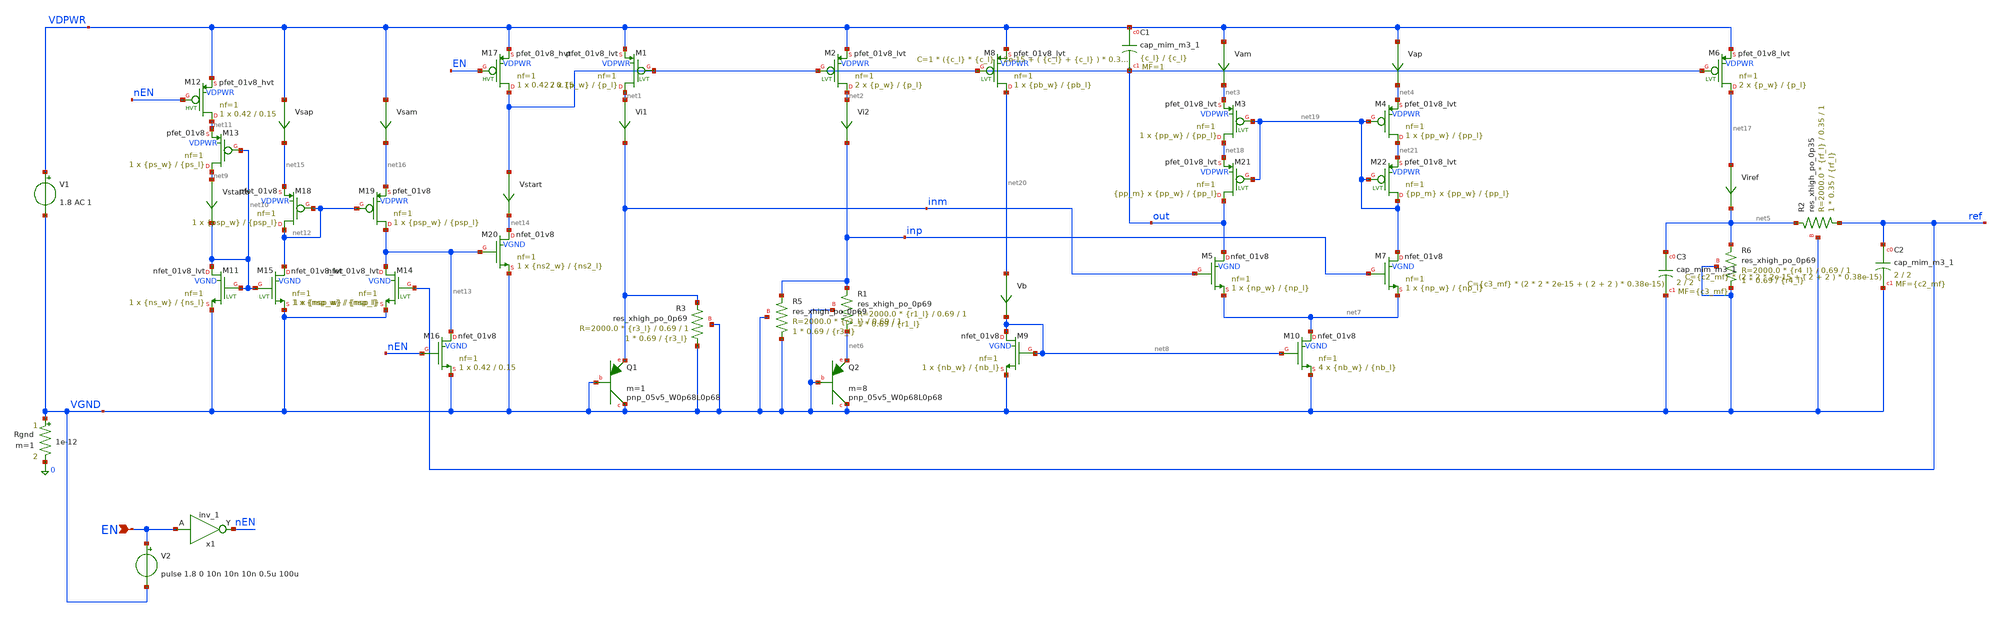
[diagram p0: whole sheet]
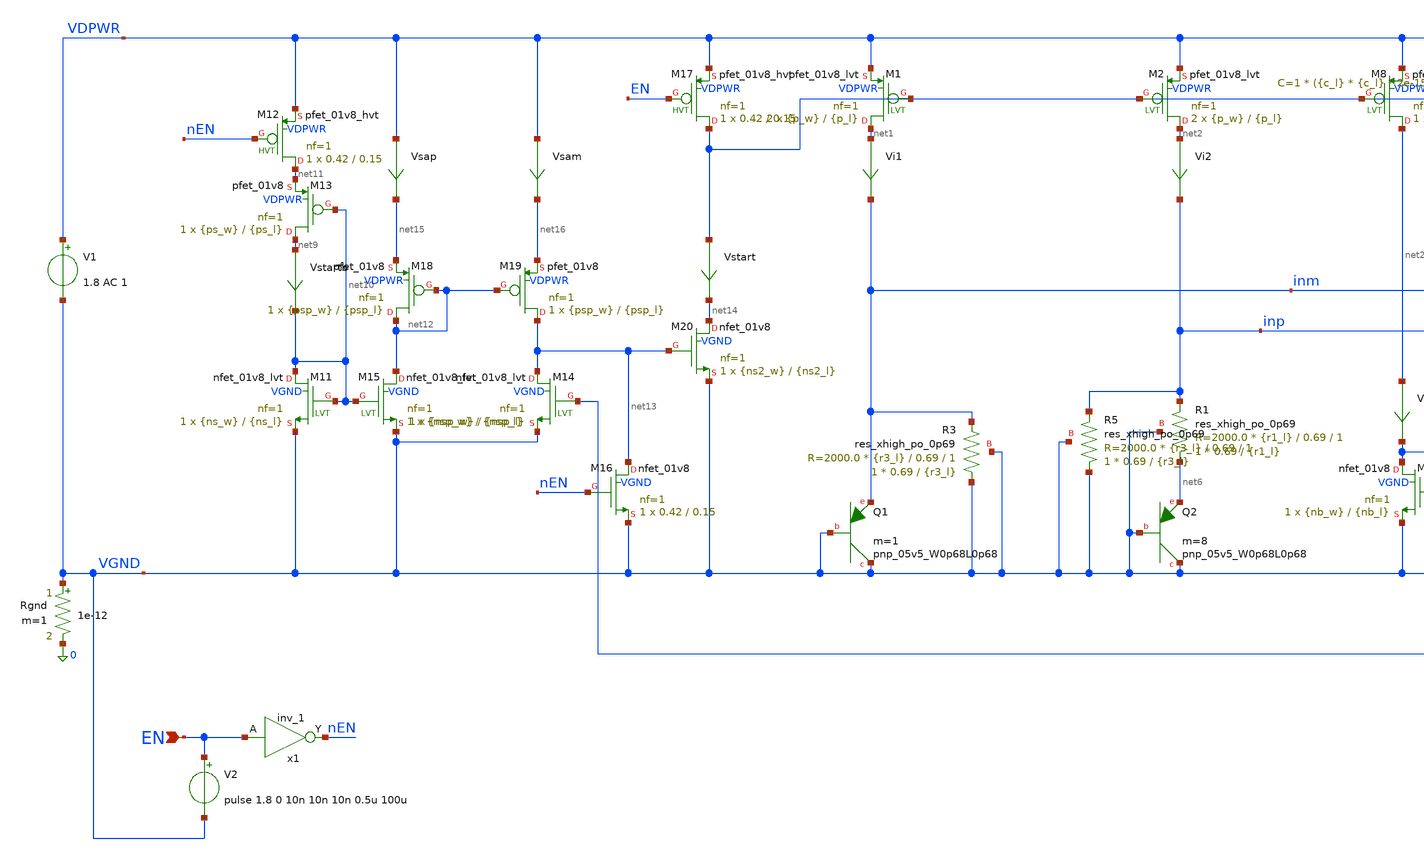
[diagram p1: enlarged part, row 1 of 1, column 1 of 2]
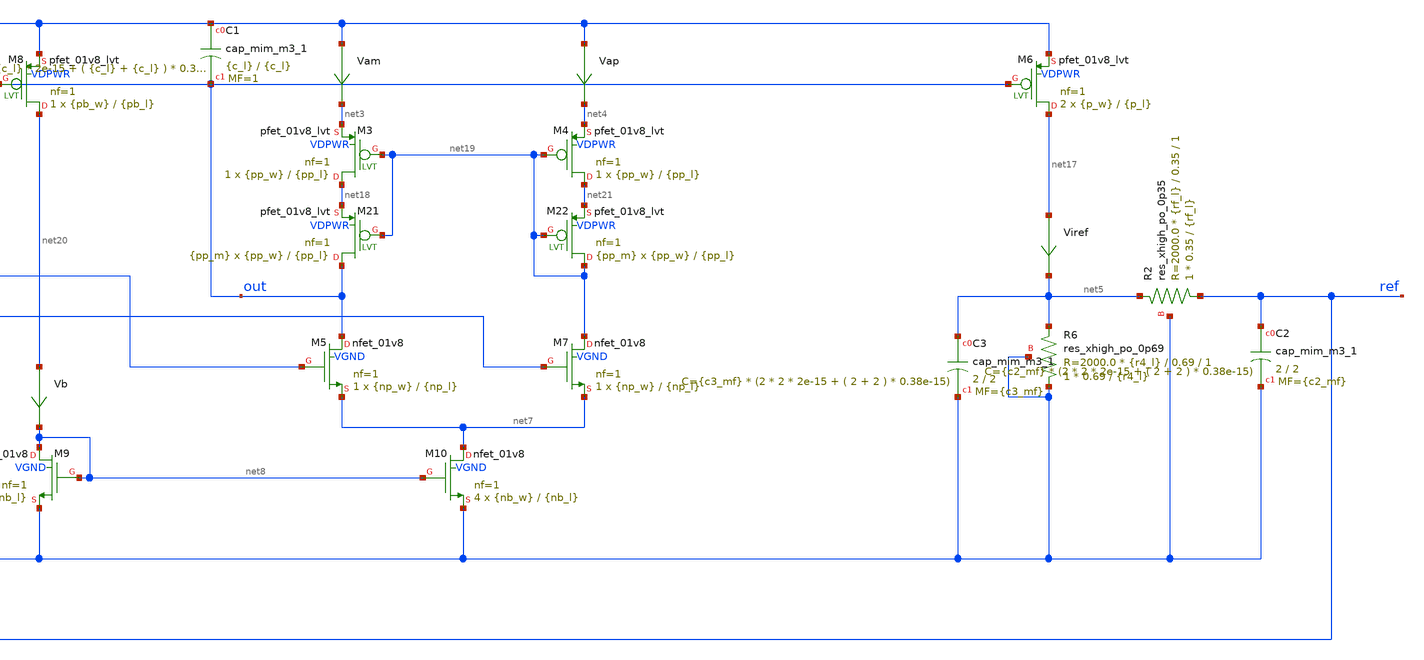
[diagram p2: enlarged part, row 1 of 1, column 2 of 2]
** sch_path: xschem/bgr.sch
**.subckt bgr EN
*.ipin EN
XQ1 VGND VGND inm sky130_fd_pr__pnp_05v5_W0p68L0p68 m=1
Rgnd VGND 0 1e-12 m=1
V1 VDPWR VGND 1.8 AC 1
XR1 net6 inp VGND sky130_fd_pr__res_xhigh_po_0p69 L={r1_l} mult=1 m=1
XQ2 VGND VGND net6 sky130_fd_pr__pnp_05v5_W0p68L0p68 m=8
XM1 net1 out VDPWR VDPWR sky130_fd_pr__pfet_01v8_lvt L={p_l} W={p_w} nf=1 ad='int((1 + 1)/2) * {p_w} / 1 * 0.29'
+ as='int((1 + 2)/2) * {p_w} / 1 * 0.29' pd='2*int((1 + 1)/2) * ({p_w} / 1 + 0.29)' ps='2*int((1 + 2)/2) * ({p_w} / 1 + 0.29)'
+ nrd='0.29 / {p_w} ' nrs='0.29 / {p_w} ' sa=0 sb=0 sd=0 mult=2 m=2
XM2 net2 out VDPWR VDPWR sky130_fd_pr__pfet_01v8_lvt L={p_l} W={p_w} nf=1 ad='int((1 + 1)/2) * {p_w} / 1 * 0.29'
+ as='int((1 + 2)/2) * {p_w} / 1 * 0.29' pd='2*int((1 + 1)/2) * ({p_w} / 1 + 0.29)' ps='2*int((1 + 2)/2) * ({p_w} / 1 + 0.29)'
+ nrd='0.29 / {p_w} ' nrs='0.29 / {p_w} ' sa=0 sb=0 sd=0 mult=2 m=2
XM3 net18 net19 net3 VDPWR sky130_fd_pr__pfet_01v8_lvt L={pp_l} W={pp_w} nf=1 ad='int((1 + 1)/2) * {pp_w} / 1 * 0.29'
+ as='int((1 + 2)/2) * {pp_w} / 1 * 0.29' pd='2*int((1 + 1)/2) * ({pp_w} / 1 + 0.29)' ps='2*int((1 + 2)/2) * ({pp_w} / 1 + 0.29)'
+ nrd='0.29 / {pp_w} ' nrs='0.29 / {pp_w} ' sa=0 sb=0 sd=0 mult=1 m=1
XM4 net21 net19 net4 VDPWR sky130_fd_pr__pfet_01v8_lvt L={pp_l} W={pp_w} nf=1 ad='int((1 + 1)/2) * {pp_w} / 1 * 0.29'
+ as='int((1 + 2)/2) * {pp_w} / 1 * 0.29' pd='2*int((1 + 1)/2) * ({pp_w} / 1 + 0.29)' ps='2*int((1 + 2)/2) * ({pp_w} / 1 + 0.29)'
+ nrd='0.29 / {pp_w} ' nrs='0.29 / {pp_w} ' sa=0 sb=0 sd=0 mult=1 m=1
XM7 net19 inp net7 VGND sky130_fd_pr__nfet_01v8 L={np_l} W={np_w} nf=1 ad='int((1 + 1)/2) * {np_w} / 1 * 0.29'
+ as='int((1 + 2)/2) * {np_w} / 1 * 0.29' pd='2*int((1 + 1)/2) * ({np_w} / 1 + 0.29)' ps='2*int((1 + 2)/2) * ({np_w} / 1 + 0.29)'
+ nrd='0.29 / {np_w} ' nrs='0.29 / {np_w} ' sa=0 sb=0 sd=0 mult=1 m=1
Vi1 net1 inm 0
.save i(vi1)
Vi2 net2 inp 0
.save i(vi2)
Vam VDPWR net3 0
.save i(vam)
Vap VDPWR net4 0
.save i(vap)
XR3 VGND inm VGND sky130_fd_pr__res_xhigh_po_0p69 L={r3_l} mult=1 m=1
XR5 VGND inp VGND sky130_fd_pr__res_xhigh_po_0p69 L={r3_l} mult=1 m=1
XM5 out inm net7 VGND sky130_fd_pr__nfet_01v8 L={np_l} W={np_w} nf=1 ad='int((1 + 1)/2) * {np_w} / 1 * 0.29'
+ as='int((1 + 2)/2) * {np_w} / 1 * 0.29' pd='2*int((1 + 1)/2) * ({np_w} / 1 + 0.29)' ps='2*int((1 + 2)/2) * ({np_w} / 1 + 0.29)'
+ nrd='0.29 / {np_w} ' nrs='0.29 / {np_w} ' sa=0 sb=0 sd=0 mult=1 m=1
XM6 net17 out VDPWR VDPWR sky130_fd_pr__pfet_01v8_lvt L={p_l} W={p_w} nf=1 ad='int((1 + 1)/2) * {p_w} / 1 * 0.29'
+ as='int((1 + 2)/2) * {p_w} / 1 * 0.29' pd='2*int((1 + 1)/2) * ({p_w} / 1 + 0.29)' ps='2*int((1 + 2)/2) * ({p_w} / 1 + 0.29)'
+ nrd='0.29 / {p_w} ' nrs='0.29 / {p_w} ' sa=0 sb=0 sd=0 mult=2 m=2
XR6 VGND net5 VGND sky130_fd_pr__res_xhigh_po_0p69 L={r4_l} mult=1 m=1
Viref net17 net5 0
.save i(viref)
XM8 net20 out VDPWR VDPWR sky130_fd_pr__pfet_01v8_lvt L={pb_l} W={pb_w} nf=1 ad='int((1 + 1)/2) * {pb_w} / 1 * 0.29'
+ as='int((1 + 2)/2) * {pb_w} / 1 * 0.29' pd='2*int((1 + 1)/2) * ({pb_w} / 1 + 0.29)' ps='2*int((1 + 2)/2) * ({pb_w} / 1 + 0.29)'
+ nrd='0.29 / {pb_w} ' nrs='0.29 / {pb_w} ' sa=0 sb=0 sd=0 mult=1 m=1
XM9 net8 net8 VGND VGND sky130_fd_pr__nfet_01v8 L={nb_l} W={nb_w} nf=1 ad='int((1 + 1)/2) * {nb_w} / 1 * 0.29'
+ as='int((1 + 2)/2) * {nb_w} / 1 * 0.29' pd='2*int((1 + 1)/2) * ({nb_w} / 1 + 0.29)' ps='2*int((1 + 2)/2) * ({nb_w} / 1 + 0.29)'
+ nrd='0.29 / {nb_w} ' nrs='0.29 / {nb_w} ' sa=0 sb=0 sd=0 mult=1 m=1
XM10 net7 net8 VGND VGND sky130_fd_pr__nfet_01v8 L={nb_l} W={nb_w} nf=1 ad='int((1 + 1)/2) * {nb_w} / 1 * 0.29'
+ as='int((1 + 2)/2) * {nb_w} / 1 * 0.29' pd='2*int((1 + 1)/2) * ({nb_w} / 1 + 0.29)' ps='2*int((1 + 2)/2) * ({nb_w} / 1 + 0.29)'
+ nrd='0.29 / {nb_w} ' nrs='0.29 / {nb_w} ' sa=0 sb=0 sd=0 mult=4 m=4
Vb net20 net8 0
.save i(vb)
XC1 VDPWR out sky130_fd_pr__cap_mim_m3_1 W={c_l} L={c_l} MF=1 m=1
x1 EN VGND VGND VDPWR VDPWR nEN sky130_fd_sc_hd__inv_1
XM15 net12 net10 VGND VGND sky130_fd_pr__nfet_01v8_lvt L={nsp_l} W={nsp_w} nf=1 ad='int((1 + 1)/2) * {nsp_w} / 1 * 0.29'
+ as='int((1 + 2)/2) * {nsp_w} / 1 * 0.29' pd='2*int((1 + 1)/2) * ({nsp_w} / 1 + 0.29)' ps='2*int((1 + 2)/2) * ({nsp_w} / 1 + 0.29)'
+ nrd='0.29 / {nsp_w} ' nrs='0.29 / {nsp_w} ' sa=0 sb=0 sd=0 mult=1 m=1
XM11 net10 net10 VGND VGND sky130_fd_pr__nfet_01v8_lvt L={ns_l} W={ns_w} nf=1 ad='int((1 + 1)/2) * {ns_w} / 1 * 0.29'
+ as='int((1 + 2)/2) * {ns_w} / 1 * 0.29' pd='2*int((1 + 1)/2) * ({ns_w} / 1 + 0.29)' ps='2*int((1 + 2)/2) * ({ns_w} / 1 + 0.29)'
+ nrd='0.29 / {ns_w} ' nrs='0.29 / {ns_w} ' sa=0 sb=0 sd=0 mult=1 m=1
Vstartb net9 net10 0
.save i(vstartb)
Vstart out net14 0
.save i(vstart)
XM13 net9 net10 net11 VDPWR sky130_fd_pr__pfet_01v8 L={ps_l} W={ps_w} nf=1 ad='int((1 + 1)/2) * {ps_w} / 1 * 0.29'
+ as='int((1 + 2)/2) * {ps_w} / 1 * 0.29' pd='2*int((1 + 1)/2) * ({ps_w} / 1 + 0.29)' ps='2*int((1 + 2)/2) * ({ps_w} / 1 + 0.29)'
+ nrd='0.29 / {ps_w} ' nrs='0.29 / {ps_w} ' sa=0 sb=0 sd=0 mult=1 m=1
XM16 net13 nEN VGND VGND sky130_fd_pr__nfet_01v8 L=0.15 W=0.42 nf=1 ad='int((1 + 1)/2) * 0.42 / 1 * 0.29'
+ as='int((1 + 2)/2) * 0.42 / 1 * 0.29' pd='2*int((1 + 1)/2) * (0.42 / 1 + 0.29)' ps='2*int((1 + 2)/2) * (0.42 / 1 + 0.29)'
+ nrd='0.29 / 0.42 ' nrs='0.29 / 0.42 ' sa=0 sb=0 sd=0 mult=1 m=1
XM17 out EN VDPWR VDPWR sky130_fd_pr__pfet_01v8_hvt L=0.15 W=0.42 nf=1 ad='int((1 + 1)/2) * 0.42 / 1 * 0.29'
+ as='int((1 + 2)/2) * 0.42 / 1 * 0.29' pd='2*int((1 + 1)/2) * (0.42 / 1 + 0.29)' ps='2*int((1 + 2)/2) * (0.42 / 1 + 0.29)'
+ nrd='0.29 / 0.42 ' nrs='0.29 / 0.42 ' sa=0 sb=0 sd=0 mult=1 m=1
XM12 net11 nEN VDPWR VDPWR sky130_fd_pr__pfet_01v8_hvt L=0.15 W=0.42 nf=1 ad='int((1 + 1)/2) * 0.42 / 1 * 0.29'
+ as='int((1 + 2)/2) * 0.42 / 1 * 0.29' pd='2*int((1 + 1)/2) * (0.42 / 1 + 0.29)' ps='2*int((1 + 2)/2) * (0.42 / 1 + 0.29)'
+ nrd='0.29 / 0.42 ' nrs='0.29 / 0.42 ' sa=0 sb=0 sd=0 mult=1 m=1
V2 EN VGND pulse 1.8 0 10n 10n 10n 0.5u 100u
XM14 net13 ref VGND VGND sky130_fd_pr__nfet_01v8_lvt L={nsp_l} W={nsp_w} nf=1 ad='int((1 + 1)/2) * {nsp_w} / 1 * 0.29'
+ as='int((1 + 2)/2) * {nsp_w} / 1 * 0.29' pd='2*int((1 + 1)/2) * ({nsp_w} / 1 + 0.29)' ps='2*int((1 + 2)/2) * ({nsp_w} / 1 + 0.29)'
+ nrd='0.29 / {nsp_w} ' nrs='0.29 / {nsp_w} ' sa=0 sb=0 sd=0 mult=1 m=1
XM18 net12 net12 net15 VDPWR sky130_fd_pr__pfet_01v8 L={psp_l} W={psp_w} nf=1 ad='int((1 + 1)/2) * {psp_w} / 1 * 0.29'
+ as='int((1 + 2)/2) * {psp_w} / 1 * 0.29' pd='2*int((1 + 1)/2) * ({psp_w} / 1 + 0.29)' ps='2*int((1 + 2)/2) * ({psp_w} / 1 + 0.29)'
+ nrd='0.29 / {psp_w} ' nrs='0.29 / {psp_w} ' sa=0 sb=0 sd=0 mult=1 m=1
XM19 net13 net12 net16 VDPWR sky130_fd_pr__pfet_01v8 L={psp_l} W={psp_w} nf=1 ad='int((1 + 1)/2) * {psp_w} / 1 * 0.29'
+ as='int((1 + 2)/2) * {psp_w} / 1 * 0.29' pd='2*int((1 + 1)/2) * ({psp_w} / 1 + 0.29)' ps='2*int((1 + 2)/2) * ({psp_w} / 1 + 0.29)'
+ nrd='0.29 / {psp_w} ' nrs='0.29 / {psp_w} ' sa=0 sb=0 sd=0 mult=1 m=1
XM20 net14 net13 VGND VGND sky130_fd_pr__nfet_01v8 L={ns2_l} W={ns2_w} nf=1 ad='int((1 + 1)/2) * {ns2_w} / 1 * 0.29'
+ as='int((1 + 2)/2) * {ns2_w} / 1 * 0.29' pd='2*int((1 + 1)/2) * ({ns2_w} / 1 + 0.29)' ps='2*int((1 + 2)/2) * ({ns2_w} / 1 + 0.29)'
+ nrd='0.29 / {ns2_w} ' nrs='0.29 / {ns2_w} ' sa=0 sb=0 sd=0 mult=1 m=1
Vsap VDPWR net15 0
.save i(vsap)
Vsam VDPWR net16 0
.save i(vsam)
XC2 ref VGND sky130_fd_pr__cap_mim_m3_1 W=2 L=2 MF={c2_mf} m={c2_mf}
XR2 ref net5 VGND sky130_fd_pr__res_xhigh_po_0p35 L={rf_l} mult=1 m=1
XC3 net5 VGND sky130_fd_pr__cap_mim_m3_1 W=2 L=2 MF={c3_mf} m={c3_mf}
XM21 out net19 net18 VDPWR sky130_fd_pr__pfet_01v8_lvt L={pp_l} W={pp_w} nf=1 ad='int((1 + 1)/2) * {pp_w} / 1 * 0.29'
+ as='int((1 + 2)/2) * {pp_w} / 1 * 0.29' pd='2*int((1 + 1)/2) * ({pp_w} / 1 + 0.29)' ps='2*int((1 + 2)/2) * ({pp_w} / 1 + 0.29)'
+ nrd='0.29 / {pp_w} ' nrs='0.29 / {pp_w} ' sa=0 sb=0 sd=0 mult={pp_m} m={pp_m}
XM22 net19 net19 net21 VDPWR sky130_fd_pr__pfet_01v8_lvt L={pp_l} W={pp_w} nf=1 ad='int((1 + 1)/2) * {pp_w} / 1 * 0.29'
+ as='int((1 + 2)/2) * {pp_w} / 1 * 0.29' pd='2*int((1 + 1)/2) * ({pp_w} / 1 + 0.29)' ps='2*int((1 + 2)/2) * ({pp_w} / 1 + 0.29)'
+ nrd='0.29 / {pp_w} ' nrs='0.29 / {pp_w} ' sa=0 sb=0 sd=0 mult={pp_m} m={pp_m}
**** begin user architecture code


.param p_l=1 p_w=4 pp_l=0.5 pp_w=2 pp_m=8 np_w=2 np_l=0.5 nb_w=1 nb_l=0.5 pb_w=0.42 pb_l=1
.param r1_l=4 r3_l=32 r4_l=20.8 c_l=2 c2_mf=4 c3_mf=4 rf_l=4
.param ps_w=0.42 ps_l=3 ns2_w=0.42 ns2_l=0.5 ns_w=0.5 ns_l=0.15 nsp_w=0.5 nsp_l=0.5 psp_w=0.5
+ psp_l=0.5
.options savecurrents
.save all
.save ref
.save inm inp
.control
let run=1
*dowhile run < 128
 dc temp -40 125 15 v1 1.6 2 0.2
 plot ref
* write bgr.raw
* set appendwrite
* reset
* let run=run+1
*end
.endc




.lib $::SKYWATER_MODELS/../ngspice/sky130.lib.spice tt
.include $::SKYWATER_MODELS/../../libs.ref/sky130_fd_sc_hd/spice/sky130_fd_sc_hd.spice


**** end user architecture code
**.ends
.end
